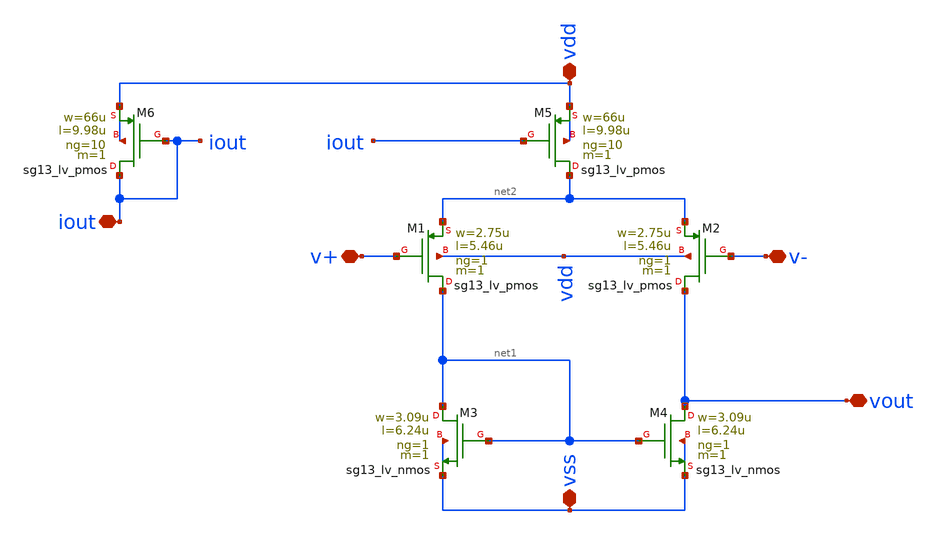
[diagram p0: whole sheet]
** sch_path: modules/module_1_bandgap_reference/part_1_OTA/gmid_example/schematic/two_stage_OTA.sch
**.subckt two_stage_OTA v- v+ vss vdd iout vout
*.iopin v-
*.iopin v+
*.iopin vss
*.iopin vdd
*.iopin iout
*.iopin vout
XM4 vout net1 vss vss sg13_lv_nmos w=3.09u l=6.24u ng=1 m=1 mm_ok=1
XM3 net1 net1 vss vss sg13_lv_nmos w=3.09u l=6.24u ng=1 m=1 mm_ok=1
XM1 net1 v+ net2 vdd sg13_lv_pmos w=2.75u l=5.46u ng=1 m=1 mm_ok=1
XM5 net2 iout vdd vdd sg13_lv_pmos w=66u l=9.98u ng=10 m=1 mm_ok=1
XM6 iout iout vdd vdd sg13_lv_pmos w=66u l=9.98u ng=10 m=1 mm_ok=1
XM2 vout v- net2 vdd sg13_lv_pmos w=2.75u l=5.46u ng=1 m=1 mm_ok=1
**.ends
.end
